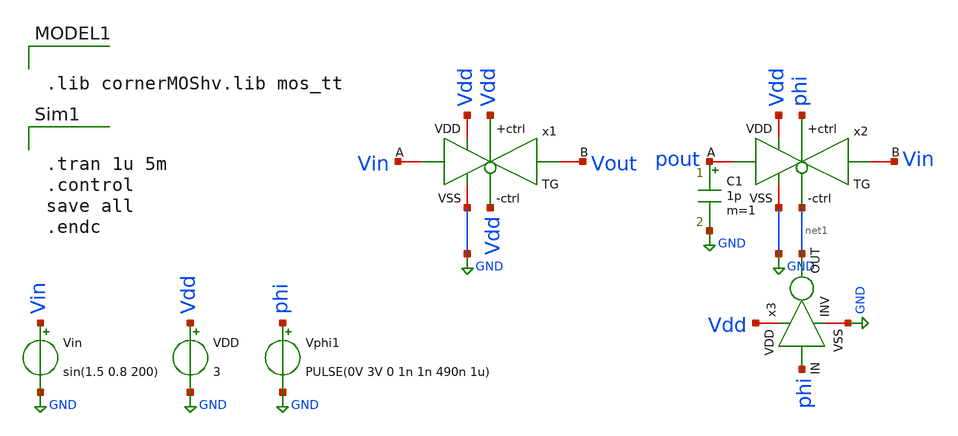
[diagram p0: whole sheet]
** sch_path: real_circuit/final/TGATE_tb.sch
**.subckt TGATE_tb
VDD Vdd GND 3
Vin Vin GND sin(1.5 0.8 200)
Vphi1 phi GND PULSE(0V 3V 0 1n 1n 490n 1u)
C1 pout GND 1p m=1
x1 Vdd Vdd Vout Vin Vdd GND TG
x2 phi Vdd Vin pout net1 GND TG
x3 Vdd phi net1 GND INV
**** begin user architecture code


.tran 1u 5m
.control
save all
.endc



.lib cornerMOShv.lib mos_tt

**** end user architecture code
**.ends

* expanding   symbol:  /foss/designs/final/TG.sym # of pins=6
** sym_path: real_circuit/final/TG.sym
** sch_path: real_circuit/final/TG.sch
.subckt TG +ctrl VDD B A -ctrl VSS
*.iopin A
*.iopin B
*.iopin VDD
*.iopin VSS
*.ipin +ctrl
*.ipin -ctrl
XM1 B -ctrl A VSS sg13_hv_nmos w=1u l=0.6u ng=1 m=1 mm_ok=1
XM2 B +ctrl A VDD sg13_hv_pmos w=2.5u l=0.6u ng=1 m=1 mm_ok=1
.ends


* expanding   symbol:  /foss/designs/final/INV.sym # of pins=4
** sym_path: real_circuit/final/INV.sym
** sch_path: real_circuit/final/INV.sch
.subckt INV VDD IN OUT VSS
*.iopin VDD
*.iopin VSS
*.ipin IN
*.opin OUT
XM1 OUT IN VDD VDD sg13_hv_pmos w=2u l=0.6u ng=1 m=1 mm_ok=1
XM2 OUT IN VSS VSS sg13_hv_nmos w=1u l=0.6u ng=1 m=1 mm_ok=1
.ends

.GLOBAL GND
.end
